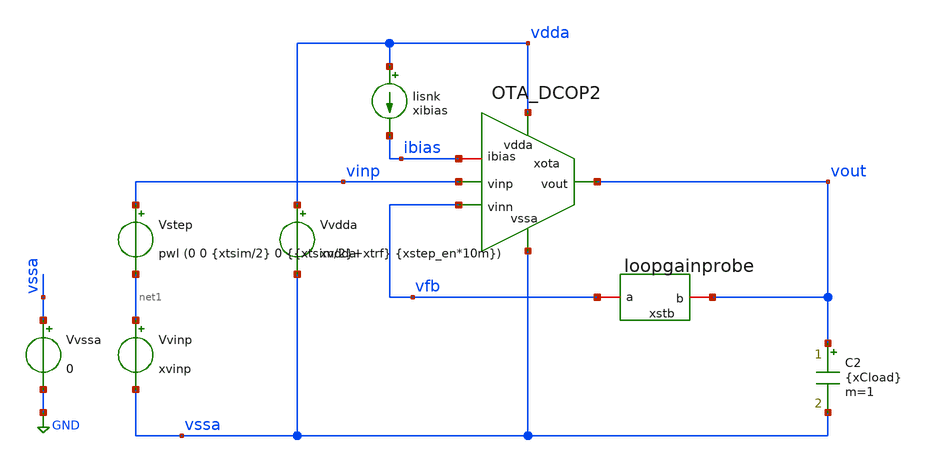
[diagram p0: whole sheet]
** sch_path: Analysing_DCOPs_in_xschem_ngpisce_in_SW130/tb_OTA.sch
**.subckt tb_OTA
Vvdda vdda vssa xvdda
Iisnk vdda ibias xibias
C2 vout vssa {xCload} m=1
xota vdda vinp vfb vssa vout ibias OTA_DCOP2
Vstep vinp net1 pwl (0 0 {xtsim/2} 0 {{xtsim/2}+xtrf} {xstep_en*10m})
Vvinp net1 vssa xvinp
Vvssa vssa GND 0
xstb vfb vout loopgainprobe
**** begin user architecture code

** opencircuitdesign pdks install
*.lib $::SKYWATER_MODELS/sky130.lib.spice tt
.lib /home/slice/pdk/SW130/share/pdk/sky130A/libs.tech/combined/sky130.lib.spice tt
*.lib /home/slice/pdk/SW130/share/pdk/sky130A/libs.tech/combined/sky130.lib.spice ss
*.lib /home/slice/pdk/SW130/share/pdk/sky130A/libs.tech/combined/sky130.lib.spice ff
*.lib /home/slice/pdk/SW130/share/pdk/sky130A/libs.tech/combined/sky130.lib.spice sf
*.lib /home/slice/pdk/SW130/share/pdk/sky130A/libs.tech/combined/sky130.lib.spice fs

* Parameters
.param xvdda = 1.8
.param xvinp = 1
.param xibias = 2u
.param xCload = 0p
.param xgm_dp = 1e-3
.param xRin = 1/xgm_dp
.param xCout = 1p
.param xRout = 1e6
.param xtrf = 50p
.param xtsim = 5u
.param xstep_en = 1

.model OTA_vcvs OTA_vcvs
* vlogA instantiation


  ** 1. DCOP analysis **
  ** must save the below for DCOP analysis to be back annotated onto the schematic
  .option savecurrents
  .save
  +  @m.xota.m1[vgs]
  +  @m.xota.m1[vth]
  +  @m.xota.m1[gds]
  +  @m.xota.m1[gm]
  +  @m.xota.m1[id]
  +  @m.xota2.m1[vgs]
  +  @m.xota2.m1[vth]
  +  @m.xota2.m1[gds]
  +  @m.xota2.m1[gm]
  +  @m.xota2.m1[id]

  +  @m.xota.m2[vgs]
  +  @m.xota.m2[vth]
  +  @m.xota.m2[gds]
  +  @m.xota.m2[gm]
  +  @m.xota.m2[id]
  +  @m.xota2.m2[vgs]
  +  @m.xota2.m2[vth]
  +  @m.xota2.m2[gds]
  +  @m.xota2.m2[gm]
  +  @m.xota2.m2[id]

  +  @m.xota.m3[vgs]
  +  @m.xota.m3[vth]
  +  @m.xota.m3[gds]
  +  @m.xota.m3[gm]
  +  @m.xota.m3[id]
  +  @m.xota2.m3[vgs]
  +  @m.xota2.m3[vth]
  +  @m.xota2.m3[gds]
  +  @m.xota2.m3[gm]
  +  @m.xota2.m3[id]

  +  @m.xota.m4[vgs]
  +  @m.xota.m4[vth]
  +  @m.xota.m4[gds]
  +  @m.xota.m4[gm]
  +  @m.xota.m4[id]
  +  @m.xota2.m4[vgs]
  +  @m.xota2.m4[vth]
  +  @m.xota2.m4[gds]
  +  @m.xota2.m4[gm]
  +  @m.xota2.m4[id]

  +  @m.xota.m5[vgs]
  +  @m.xota.m5[vth]
  +  @m.xota.m5[gds]
  +  @m.xota.m5[gm]
  +  @m.xota.m5[id]
  +  @m.xota2.m5[vgs]
  +  @m.xota2.m5[vth]
  +  @m.xota2.m5[gds]
  +  @m.xota2.m5[gm]
  +  @m.xota2.m5[id]

*  +  @m.xota.m6[vgs]
  +  @m.xota.xm6.msky130_fd_pr__pfet_01v8[vgs]
*  +  @m.xota.m6[vds]
  +  @m.xota.xm6.msky130_fd_pr__pfet_01v8[vds]
*  +  @m.xota.m6[vth]
  +  @m.xota.xm6.msky130_fd_pr__pfet_01v8[vth]
*  +  @m.xota.m6[gds]
  +  @m.xota.xm6.msky130_fd_pr__pfet_01v8[gds]
*  +  @m.xota.m6[gm]
  +  @m.xota.xm6.msky130_fd_pr__pfet_01v8[gm]
*  +  @m.xota.m6[id]
  +  @m.xota.xm6.msky130_fd_pr__pfet_01v8[id]
*  +  @m.xota.m6[vdsat]
  +  @m.xota.xm6.msky130_fd_pr__pfet_01v8[vdsat]
  +  @m.xota2.m6vgs]
  +  @m.xota2.m6[vth]
  +  @m.xota2.m6[gds]
  +  @m.xota2.m6[gm]
  +  @m.xota2.m6[id]

  .control
  let xtsim = 5u
  pre_osdi OTA_vcvs.osdi
  save all

  op
  write tb_ota_1stage_op.raw

** 2. TRAN ANALYSIS **

  remzerovec
  set appendwrite
  tran 1n $&xtsim
  write tb_ota_1stage_op.raw
 * write tb_ota_1stage_tran.raw
 * plot v(vout) v(vinp) v(vdda)
 unset appendwrite

** 3. AC ANALYSIS **

  alter i.xstb.Ii acmag=0
  alter v.xstb.Vi acmag=1

  ac dec 10 1 100G
  remzerovec

*  unset appendwrite

  write tb_OTA_1stage_ac1.raw

  alter i.xstb.Ii acmag=1
  alter v.xstb.Vi acmag=0

  ac dec 10 1 100G

  * use this line if you want the phase response to start at 180deg
  *let av = {1/(1-1/(2*(ac1.i(v.xstb.Vi)*ac2.v(xstb.x)-ac1.v(xstb.x)*ac2.i(v.xstb.Vi))+ac1.v(xstb.x)+ac2.i(v.xstb.Vi)))}

  * use this line if you want the phase response to start at 0deg (more conventional and directly
+ corresponds to Franks derivation)
  let av = {1/(1/(2*(ac1.i(v.xstb.Vi)*ac2.v(xstb.x)-ac1.v(xstb.x)*ac2.i(v.xstb.Vi))+ac1.v(xstb.x)+ac2.i(v.xstb.Vi))-1)}

  remzerovec
  write tb_OTA_1stage_ac2.raw

  *ngspice plots
  *plot vdb(av) xlog
  *plot {(180/pi)*vp(av)} xlog
  *plot 180*cph(av)/pi

  ** 4. MEASURES **

  let n45_rads = -45*(pi/180)
  meas AC Av_0 FIND vdb(av) AT=10
  echo --
  meas AC BW WHEN vp(av)=n45_rads CROSS=1
  echo --
  meas AC Av_BW FIND vdb(av) WHEN vp(av)=n45_rads CROSS=1
  echo --
  meas AC ULGF WHEN vdb(av)=0
  echo --
  meas AC ULGF_phi_rads FIND vp(av) WHEN vdb(av)=0 CROSS=1
  let ULGF_phi_deg = ULGF_phi_rads*(180/pi)
  print ULGF_phi_deg
  let PM = 180+ULGF_phi_deg
  print PM
  echo --
  * putting in -170 since this is a 2nd-order system so doesnt ever achieve -180
  let n180_rads = -170*(pi/180)
  meas AC GM FIND vdb(av) WHEN vp(av)=n180_rads CROSS=1

  setplot

.endc




**** end user architecture code
**.ends
.GLOBAL GND
.end
